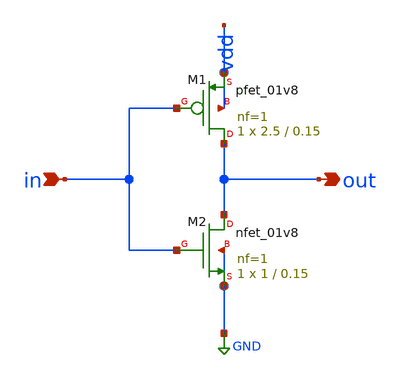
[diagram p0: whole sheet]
** sch_path: xschem/inv.sch
**.subckt inv in out
*.ipin in
*.opin out
XM1 out in vdd vdd sky130_fd_pr__pfet_01v8 L=0.15 W=2.5 nf=1 ad='int((1 + 1)/2) * 2.5 / 1 * 0.29' as='int((1 + 2)/2) * 2.5 / 1 * 0.29'
+ pd='2*int((1 + 1)/2) * (2.5 / 1 + 0.29)' ps='2*int((1 + 2)/2) * (2.5 / 1 + 0.29)' nrd='0.29 / 2.5 ' nrs='0.29 / 2.5 '
+ sa=0 sb=0 sd=0 mult=1 m=1
XM2 out in GND GND sky130_fd_pr__nfet_01v8 L=0.15 W=1 nf=1 ad='int((1 + 1)/2) * 1 / 1 * 0.29' as='int((1 + 2)/2) * 1 / 1 * 0.29'
+ pd='2*int((1 + 1)/2) * (1 / 1 + 0.29)' ps='2*int((1 + 2)/2) * (1 / 1 + 0.29)' nrd='0.29 / 1 ' nrs='0.29 / 1 '
+ sa=0 sb=0 sd=0 mult=1 m=1
**.ends
.GLOBAL GND
.end
